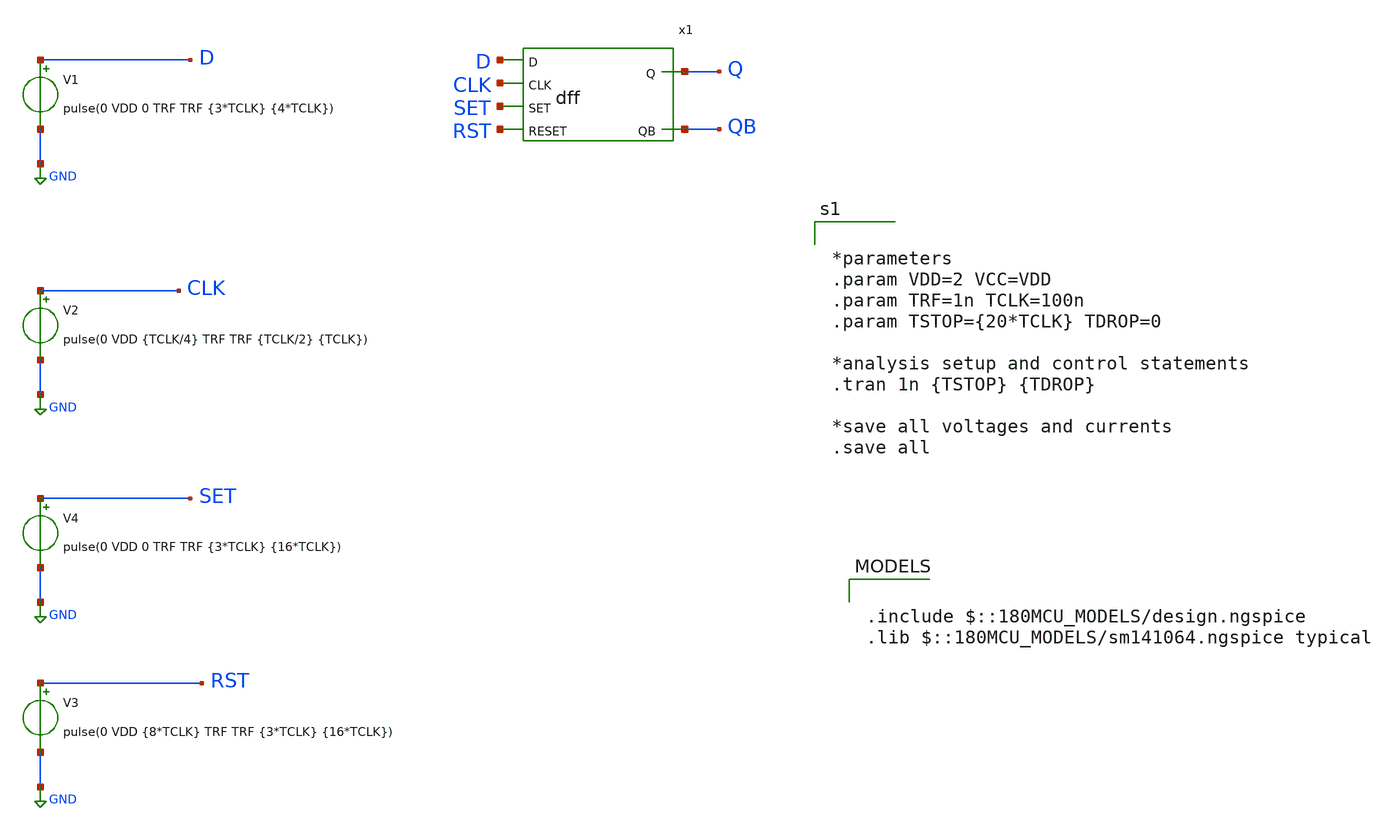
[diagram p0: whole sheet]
** sch_path: XSCHEM Files/dff_tb.sch
**.subckt dff_tb
V1 D GND pulse(0 VDD 0 TRF TRF {3*TCLK} {4*TCLK})
V2 CLK GND pulse(0 VDD {TCLK/4} TRF TRF {TCLK/2} {TCLK})
V4 SET GND pulse(0 VDD 0 TRF TRF {3*TCLK} {16*TCLK})
V3 RST GND pulse(0 VDD {8*TCLK} TRF TRF {3*TCLK} {16*TCLK})
x1 D CLK SET RST Q QB dff
**** begin user architecture code


*parameters
.param VDD=2 VCC=VDD
.param TRF=1n TCLK=100n
.param TSTOP={20*TCLK} TDROP=0

*analysis setup and control statements
.tran 1n {TSTOP} {TDROP}

*save all voltages and currents
.save all



.include $::180MCU_MODELS/design.ngspice
.lib $::180MCU_MODELS/sm141064.ngspice typical

**** end user architecture code
**.ends

* expanding   symbol:  /home/tare/Desktop/Final/dff.sym # of pins=6
** sym_path: XSCHEM Files/dff.sym
** sch_path: XSCHEM Files/dff.sch
.subckt dff D CLK SET RESET Q QB
*.ipin D
*.opin Q
*.ipin CLK
*.ipin SET
*.ipin RESET
*.opin QB
**** begin user architecture code


*nor model
a1 D CLK SET RESET OUT OUTI my_dff
.model my_dff d_dff(clk_delay = 13.0e-9 set_delay = 25.0e-9                    reset_delay = 27.0e-9
+ ic = 2 rise_delay = 10.0e-9                    fall_delay = 3e-9)

*force netlisting of digital outputs
v1 OUT Q 0
v2 OUTI QB 1


**** end user architecture code
.ends

.GLOBAL GND
.end
